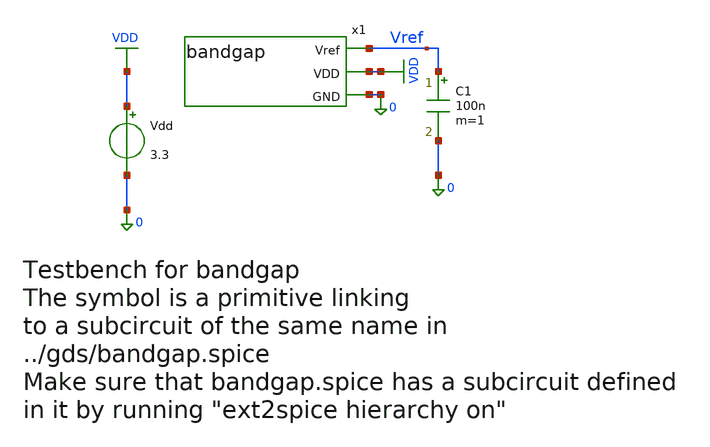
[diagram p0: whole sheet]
** sch_path: xschem/bandgap_tb.sch
* Copyright 2021 Stefan Frederik Schippers
* Licensed under the Apache License, Version 2.0 (the "License");
* you may not use this file except in compliance with the License.
* You may obtain a copy of the License at
* https://www.apache.org/licenses/LICENSE-2.0
* Unless required by applicable law or agreed to in writing, software
* distributed under the License is distributed on an "AS IS" BASIS,
* WITHOUT WARRANTIES OR CONDITIONS OF ANY KIND, either express or implied.
* See the License for the specific language governing permissions and
* limitations under the License.
**.subckt bandgap_tb
Vdd VDD 0 3.3
C1 Vref 0 100n m=1
x1 Vref VDD 0 bandgap
**** begin user architecture code

** opencircuitdesign pdks install
.lib $::SKYWATER_MODELS/sky130.lib.spice tt



.option wnflag=1
.include ../gds/bandgap.spice
.save all
.control
set gnuplot_terminal=png/quit

op
#print x1.Vg1 x1.ve1 x1.vg10 x1.vg12 x1.vg2 x1.vg3 x1.vg5 x1.vs5
#tran 10n 10u
#plot V(Vref) title 'Vref vs time'

dc VDD 3.0 3.5 0.1
gnuplot bandgap_vref_vs_vdd V(Vref)  title 'Vref vs Vdd'  xlabel 'VDD' ylabel 'Vref'
#plot V(Vref) vs V(Vdd) title 'Vref vs Vdd'

dc VDD 3.0 3.5 0.02 TEMP -40 40 20
gnuplot bandgap_vref_vs_vdd_vs_temp V(Vref)  title 'Vref vs Vdd vs Temp (-40 to 40C)'  xlabel 'VDD' ylabel
+ 'Vref'
#plot V(Vref) Vs V(Vdd) title 'Vref vs Vdd vs Temp'

#dc TEMP -40 40 10
#plot V(Vref) title 'Vref vs Temp at VDD=3.3'
quit
.endc


**** end user architecture code
**.ends
.GLOBAL VDD
.end
